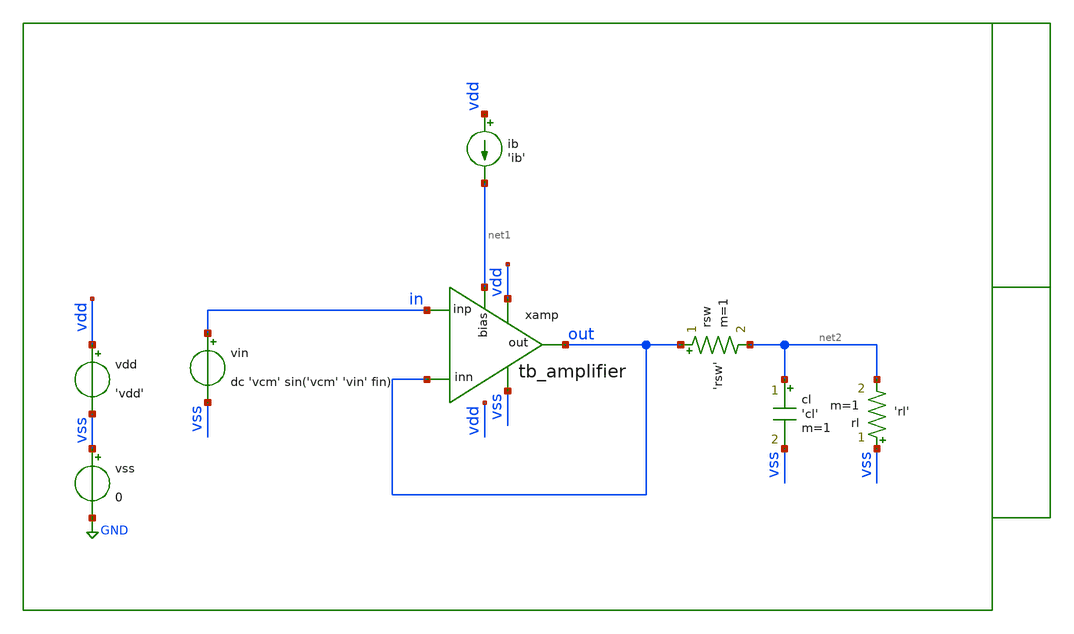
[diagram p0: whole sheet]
** sch_path: xschem/tb/testbuffer/tb_amplifier/tr_tb_amplifier.sch
**.subckt tr_tb_amplifier
vin in vss dc 'vcm' sin('vcm' 'vin' fin)
ib vdd net1 'ib'
cl net2 vss 'cl' m=1
rl vss net2 'rl' m=1
vdd vdd vss 'vdd'
vss vss GND 0
xamp vdd out in out vss net1 tb_amplifier
rsw out net2 'rsw' m=1
**** begin user architecture code
 * Control

.param vdd=3.3
.param vcm='vdd/2'
.param vin='0.1*vdd'
.param fin=10k
.param ib=5u
.param cl=10p
.param rl=1e6
.param rsw=1

.control

save all
tran 1u 3.7m
gnuplot p1 in out

meas tran out_max max v(out)
meas tran out_min min v(out)
print out_max
print out_min
set wr_singlescale
set wr_vecnames
wrdata data.csv out
.endc

 * Model Corners

.include $::CORNERS/ngspice/tt.spice
*.include $::CORNERS/ngspice/ff.spice
*.include $::CORNERS/ngspice/ss.spice
*.include $::CORNERS/ngspice/sf.spice
*.include $::CORNERS/ngspice/fs.spice

**** end user architecture code
**.ends

* expanding   symbol:  sch/testbuffer/tb_amplifier/tb_amplifier.sym # of pins=6
** sym_path: xschem/sch/testbuffer/tb_amplifier/tb_amplifier.sym
** sch_path: xschem/sch/testbuffer/tb_amplifier/tb_amplifier.sch
.subckt tb_amplifier vdd out inp inn vss bias
*.ipin inn
*.ipin inp
*.opin out
*.iopin bias
*.iopin vdd
*.iopin vss
XM3 mirr mirr vdd vdd pfet_06v0 L=4u W=16u nf=2 ad='int((nf+1)/2) * W/nf * 0.18u' as='int((nf+2)/2) * W/nf * 0.18u'
+ pd='2*int((nf+1)/2) * (W/nf + 0.18u)' ps='2*int((nf+2)/2) * (W/nf + 0.18u)' nrd='0.18u / W' nrs='0.18u / W'
+ sa=0 sb=0 sd=0 m=2 par=2
XM4 comp mirr vdd vdd pfet_06v0 L=4u W=16u nf=2 ad='int((nf+1)/2) * W/nf * 0.18u' as='int((nf+2)/2) * W/nf * 0.18u'
+ pd='2*int((nf+1)/2) * (W/nf + 0.18u)' ps='2*int((nf+2)/2) * (W/nf + 0.18u)' nrd='0.18u / W' nrs='0.18u / W'
+ sa=0 sb=0 sd=0 m=2 par=2
XM2 comp inp vcm vss nfet_06v0 L=2u W=16u nf=2 ad='int((nf+1)/2) * W/nf * 0.18u' as='int((nf+2)/2) * W/nf * 0.18u'
+ pd='2*int((nf+1)/2) * (W/nf + 0.18u)' ps='2*int((nf+2)/2) * (W/nf + 0.18u)' nrd='0.18u / W' nrs='0.18u / W'
+ sa=0 sb=0 sd=0 m=2 par=2
XM1 mirr inn vcm vss nfet_06v0 L=2u W=16u nf=2 ad='int((nf+1)/2) * W/nf * 0.18u' as='int((nf+2)/2) * W/nf * 0.18u'
+ pd='2*int((nf+1)/2) * (W/nf + 0.18u)' ps='2*int((nf+2)/2) * (W/nf + 0.18u)' nrd='0.18u / W' nrs='0.18u / W'
+ sa=0 sb=0 sd=0 m=2 par=2
XM5 vcm bias vss vss nfet_06v0 L=1u W=16u nf=2 ad='int((nf+1)/2) * W/nf * 0.18u' as='int((nf+2)/2) * W/nf * 0.18u'
+ pd='2*int((nf+1)/2) * (W/nf + 0.18u)' ps='2*int((nf+2)/2) * (W/nf + 0.18u)' nrd='0.18u / W' nrs='0.18u / W'
+ sa=0 sb=0 sd=0 m=2 par=2
XM6 out bias vss vss nfet_06v0 L=1u W=16u nf=2 ad='int((nf+1)/2) * W/nf * 0.18u' as='int((nf+2)/2) * W/nf * 0.18u'
+ pd='2*int((nf+1)/2) * (W/nf + 0.18u)' ps='2*int((nf+2)/2) * (W/nf + 0.18u)' nrd='0.18u / W' nrs='0.18u / W'
+ sa=0 sb=0 sd=0 m=12 par=12
XM7 out comp vdd vdd pfet_06v0 L=1u W=96u nf=12 ad='int((nf+1)/2) * W/nf * 0.18u' as='int((nf+2)/2) * W/nf * 0.18u'
+ pd='2*int((nf+1)/2) * (W/nf + 0.18u)' ps='2*int((nf+2)/2) * (W/nf + 0.18u)' nrd='0.18u / W' nrs='0.18u / W'
+ sa=0 sb=0 sd=0 m=1 par=1
XMB1 bias bias vss vss nfet_06v0 L=1u W=16u nf=2 ad='int((nf+1)/2) * W/nf * 0.18u' as='int((nf+2)/2) * W/nf * 0.18u'
+ pd='2*int((nf+1)/2) * (W/nf + 0.18u)' ps='2*int((nf+2)/2) * (W/nf + 0.18u)' nrd='0.18u / W' nrs='0.18u / W'
+ sa=0 sb=0 sd=0 m=2 par=2
XMB2 vbm bias vss vss nfet_06v0 L=1u W=16u nf=2 ad='int((nf+1)/2) * W/nf * 0.18u' as='int((nf+2)/2) * W/nf * 0.18u'
+ pd='2*int((nf+1)/2) * (W/nf + 0.18u)' ps='2*int((nf+2)/2) * (W/nf + 0.18u)' nrd='0.18u / W' nrs='0.18u / W'
+ sa=0 sb=0 sd=0 m=2 par=2
XMB3 vbm vbm vbt vdd pfet_06v0 L=1u W=16u nf=2 ad='int((nf+1)/2) * W/nf * 0.18u' as='int((nf+2)/2) * W/nf * 0.18u'
+ pd='2*int((nf+1)/2) * (W/nf + 0.18u)' ps='2*int((nf+2)/2) * (W/nf + 0.18u)' nrd='0.18u / W' nrs='0.18u / W'
+ sa=0 sb=0 sd=0 m=1 par=1
XMB4 vbt vbt vdd vdd pfet_06v0 L=1u W=16u nf=2 ad='int((nf+1)/2) * W/nf * 0.18u' as='int((nf+2)/2) * W/nf * 0.18u'
+ pd='2*int((nf+1)/2) * (W/nf + 0.18u)' ps='2*int((nf+2)/2) * (W/nf + 0.18u)' nrd='0.18u / W' nrs='0.18u / W'
+ sa=0 sb=0 sd=0 m=1 par=1
XRCC gc comp vdd ppolyf_u_1k_6p0 r_width=2e-6 r_length=38e-6 s=1 m=1
XMDUM1 vss vss vss vss nfet_06v0 L=2u W=16u nf=2 ad='int((nf+1)/2) * W/nf * 0.18u' as='int((nf+2)/2) * W/nf * 0.18u'
+ pd='2*int((nf+1)/2) * (W/nf + 0.18u)' ps='2*int((nf+2)/2) * (W/nf + 0.18u)' nrd='0.18u / W' nrs='0.18u / W'
+ sa=0 sb=0 sd=0 m=2 par=2
XMDUM2 vdd vdd vdd vdd pfet_06v0 L=4u W=16u nf=2 ad='int((nf+1)/2) * W/nf * 0.18u' as='int((nf+2)/2) * W/nf * 0.18u'
+ pd='2*int((nf+1)/2) * (W/nf + 0.18u)' ps='2*int((nf+2)/2) * (W/nf + 0.18u)' nrd='0.18u / W' nrs='0.18u / W'
+ sa=0 sb=0 sd=0 m=4 par=4
XC1 out gc cap_mim_2f0_m4m5_noshield c_width=30e-6 c_length=30e-6 m=1
.ends

.GLOBAL GND
.end
